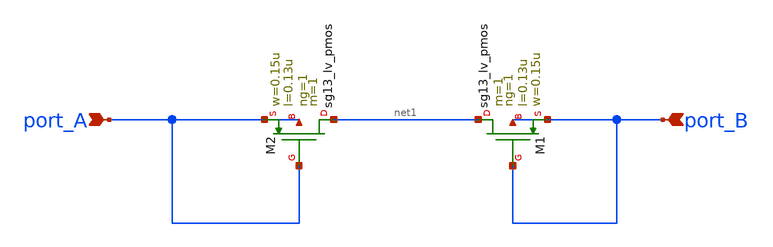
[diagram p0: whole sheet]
** sch_path: analog-db/templates/pseudo_resistor/pseudo-resistor-a-independant-well-generator.sch
* Copyright 2026 MacAnalog Research Group
**.subckt pseudo-resistor-a-independant-well-generator port_A port_B
*.ipin port_A
*.ipin port_B
XM1 net1 port_B port_B port_B sg13_lv_pmos w=0.15u l=0.13u ng=1 m=1 mm_ok=1
XM2 net1 port_A port_A port_A sg13_lv_pmos w=0.15u l=0.13u ng=1 m=1 mm_ok=1
**.ends
.end
